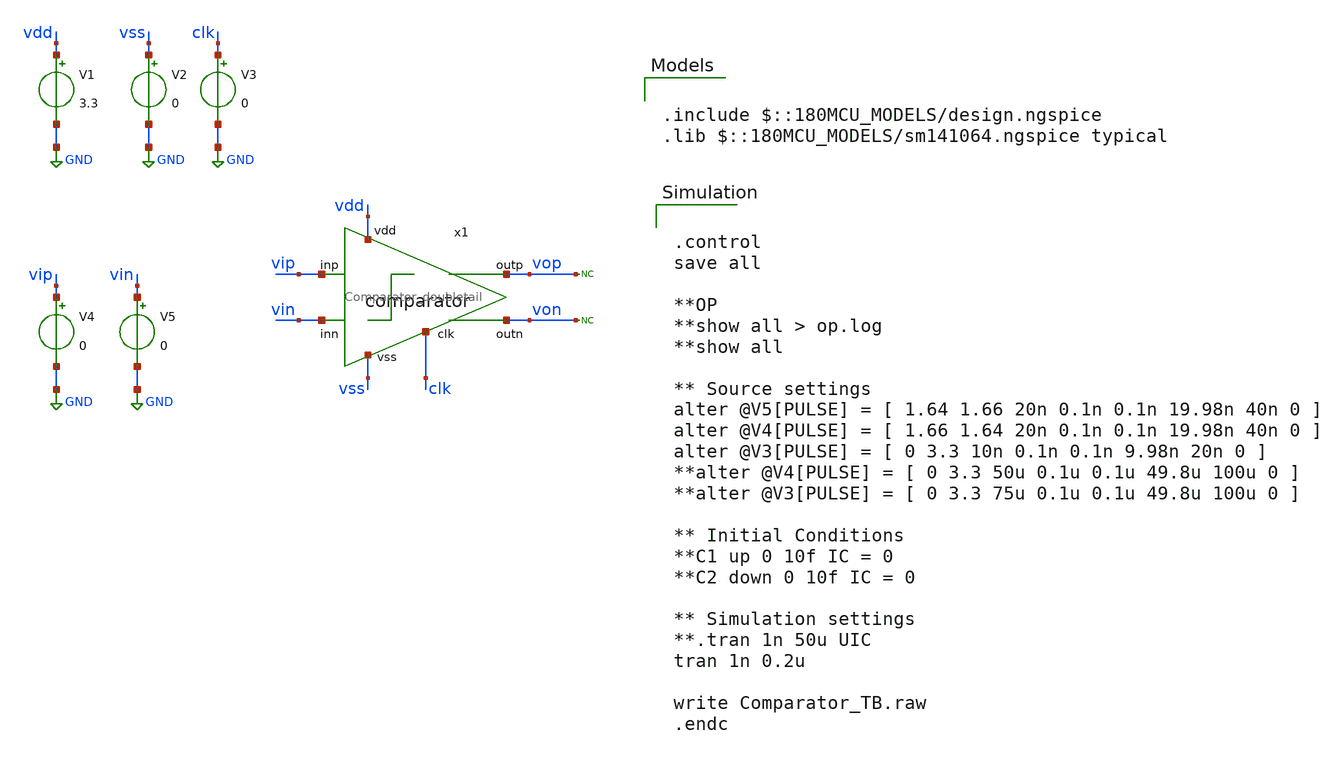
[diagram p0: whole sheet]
** sch_path: designs/Comparator_TB.sch
**.subckt Comparator_TB
V1 vdd GND 3.3
V2 vss GND 0
* noconn vop
* noconn von
V3 clk GND 0
V4 vip GND 0
V5 vin GND 0
x1 vdd clk vip vin vop von vss Comparator_doubletail
**** begin user architecture code

.include $::180MCU_MODELS/design.ngspice
.lib $::180MCU_MODELS/sm141064.ngspice typical



.control
save all

**OP
**show all > op.log
**show all

** Source settings
alter @V5[PULSE] = [ 1.64 1.66 20n 0.1n 0.1n 19.98n 40n 0 ]
alter @V4[PULSE] = [ 1.66 1.64 20n 0.1n 0.1n 19.98n 40n 0 ]
alter @V3[PULSE] = [ 0 3.3 10n 0.1n 0.1n 9.98n 20n 0 ]
**alter @V4[PULSE] = [ 0 3.3 50u 0.1u 0.1u 49.8u 100u 0 ]
**alter @V3[PULSE] = [ 0 3.3 75u 0.1u 0.1u 49.8u 100u 0 ]

** Initial Conditions
**C1 up 0 10f IC = 0
**C2 down 0 10f IC = 0

** Simulation settings
**.tran 1n 50u UIC
tran 1n 0.2u

write Comparator_TB.raw
.endc


**** end user architecture code
**.ends

* expanding   symbol:  Comparator_doubletail.sym # of pins=7
** sym_path: designs/libs/qw_core_analog_pkedit/Comparator_doubletail.sym
** sch_path: designs/libs/qw_core_analog_pkedit/Comparator_doubletail.sch
.subckt Comparator_doubletail vdd clk inp inn outp outn vss
*.iopin vdd
*.iopin vss
*.iopin clk
*.iopin inp
*.iopin inn
*.iopin outp
*.iopin outn
XM1 sigp clk vdd vdd pfet_03v3 L=0.7u W=5u nf=1 ad='int((nf+1)/2) * W/nf * 0.18u' as='int((nf+2)/2) * W/nf * 0.18u'
+ pd='2*int((nf+1)/2) * (W/nf + 0.18u)' ps='2*int((nf+2)/2) * (W/nf + 0.18u)' nrd='0.18u / W' nrs='0.18u / W'
+ sa=0 sb=0 sd=0 m=1
XM2 sign inp net1 net1 nfet_03v3 L=0.7u W=5u nf=1 ad='int((nf+1)/2) * W/nf * 0.18u' as='int((nf+2)/2) * W/nf * 0.18u'
+ pd='2*int((nf+1)/2) * (W/nf + 0.18u)' ps='2*int((nf+2)/2) * (W/nf + 0.18u)' nrd='0.18u / W' nrs='0.18u / W'
+ sa=0 sb=0 sd=0 m=1
XM3 sign clk vdd vdd pfet_03v3 L=0.7u W=5u nf=1 ad='int((nf+1)/2) * W/nf * 0.18u' as='int((nf+2)/2) * W/nf * 0.18u'
+ pd='2*int((nf+1)/2) * (W/nf + 0.18u)' ps='2*int((nf+2)/2) * (W/nf + 0.18u)' nrd='0.18u / W' nrs='0.18u / W'
+ sa=0 sb=0 sd=0 m=1
XM4 sigp inn net1 net1 nfet_03v3 L=0.7u W=5u nf=1 ad='int((nf+1)/2) * W/nf * 0.18u' as='int((nf+2)/2) * W/nf * 0.18u'
+ pd='2*int((nf+1)/2) * (W/nf + 0.18u)' ps='2*int((nf+2)/2) * (W/nf + 0.18u)' nrd='0.18u / W' nrs='0.18u / W'
+ sa=0 sb=0 sd=0 m=1
XM5 net1 clk vss vss nfet_03v3 L=0.7u W=5u nf=1 ad='int((nf+1)/2) * W/nf * 0.18u' as='int((nf+2)/2) * W/nf * 0.18u'
+ pd='2*int((nf+1)/2) * (W/nf + 0.18u)' ps='2*int((nf+2)/2) * (W/nf + 0.18u)' nrd='0.18u / W' nrs='0.18u / W'
+ sa=0 sb=0 sd=0 m=1
XM6 outp sign vss vss nfet_03v3 L=0.35u W=2.5u nf=1 ad='int((nf+1)/2) * W/nf * 0.18u' as='int((nf+2)/2) * W/nf * 0.18u'
+ pd='2*int((nf+1)/2) * (W/nf + 0.18u)' ps='2*int((nf+2)/2) * (W/nf + 0.18u)' nrd='0.18u / W' nrs='0.18u / W'
+ sa=0 sb=0 sd=0 m=1
XM7 outp outn vss vss nfet_03v3 L=0.35u W=2.5u nf=1 ad='int((nf+1)/2) * W/nf * 0.18u' as='int((nf+2)/2) * W/nf * 0.18u'
+ pd='2*int((nf+1)/2) * (W/nf + 0.18u)' ps='2*int((nf+2)/2) * (W/nf + 0.18u)' nrd='0.18u / W' nrs='0.18u / W'
+ sa=0 sb=0 sd=0 m=1
XM10 outp outn net2 vdd pfet_03v3 L=0.35u W=2.5u nf=1 ad='int((nf+1)/2) * W/nf * 0.18u' as='int((nf+2)/2) * W/nf * 0.18u'
+ pd='2*int((nf+1)/2) * (W/nf + 0.18u)' ps='2*int((nf+2)/2) * (W/nf + 0.18u)' nrd='0.18u / W' nrs='0.18u / W'
+ sa=0 sb=0 sd=0 m=1
XM11 net2 sign vdd vdd pfet_03v3 L=0.35u W=2.5u nf=1 ad='int((nf+1)/2) * W/nf * 0.18u' as='int((nf+2)/2) * W/nf * 0.18u'
+ pd='2*int((nf+1)/2) * (W/nf + 0.18u)' ps='2*int((nf+2)/2) * (W/nf + 0.18u)' nrd='0.18u / W' nrs='0.18u / W'
+ sa=0 sb=0 sd=0 m=1
XM12 net2 sign vss vss nfet_03v3 L=0.35u W=2.5u nf=1 ad='int((nf+1)/2) * W/nf * 0.18u' as='int((nf+2)/2) * W/nf * 0.18u'
+ pd='2*int((nf+1)/2) * (W/nf + 0.18u)' ps='2*int((nf+2)/2) * (W/nf + 0.18u)' nrd='0.18u / W' nrs='0.18u / W'
+ sa=0 sb=0 sd=0 m=1
XM8 outn sigp vss vss nfet_03v3 L=0.35u W=2.5u nf=1 ad='int((nf+1)/2) * W/nf * 0.18u' as='int((nf+2)/2) * W/nf * 0.18u'
+ pd='2*int((nf+1)/2) * (W/nf + 0.18u)' ps='2*int((nf+2)/2) * (W/nf + 0.18u)' nrd='0.18u / W' nrs='0.18u / W'
+ sa=0 sb=0 sd=0 m=1
XM9 outn outp vss vss nfet_03v3 L=0.35u W=2.5u nf=1 ad='int((nf+1)/2) * W/nf * 0.18u' as='int((nf+2)/2) * W/nf * 0.18u'
+ pd='2*int((nf+1)/2) * (W/nf + 0.18u)' ps='2*int((nf+2)/2) * (W/nf + 0.18u)' nrd='0.18u / W' nrs='0.18u / W'
+ sa=0 sb=0 sd=0 m=1
XM13 outn outp net3 vdd pfet_03v3 L=0.35u W=2.5u nf=1 ad='int((nf+1)/2) * W/nf * 0.18u' as='int((nf+2)/2) * W/nf * 0.18u'
+ pd='2*int((nf+1)/2) * (W/nf + 0.18u)' ps='2*int((nf+2)/2) * (W/nf + 0.18u)' nrd='0.18u / W' nrs='0.18u / W'
+ sa=0 sb=0 sd=0 m=1
XM14 net3 sigp vdd vdd pfet_03v3 L=0.35u W=2.5u nf=1 ad='int((nf+1)/2) * W/nf * 0.18u' as='int((nf+2)/2) * W/nf * 0.18u'
+ pd='2*int((nf+1)/2) * (W/nf + 0.18u)' ps='2*int((nf+2)/2) * (W/nf + 0.18u)' nrd='0.18u / W' nrs='0.18u / W'
+ sa=0 sb=0 sd=0 m=1
XM15 net3 sigp vss vss nfet_03v3 L=0.35u W=2.5u nf=1 ad='int((nf+1)/2) * W/nf * 0.18u' as='int((nf+2)/2) * W/nf * 0.18u'
+ pd='2*int((nf+1)/2) * (W/nf + 0.18u)' ps='2*int((nf+2)/2) * (W/nf + 0.18u)' nrd='0.18u / W' nrs='0.18u / W'
+ sa=0 sb=0 sd=0 m=1
.ends

.GLOBAL GND
.end
